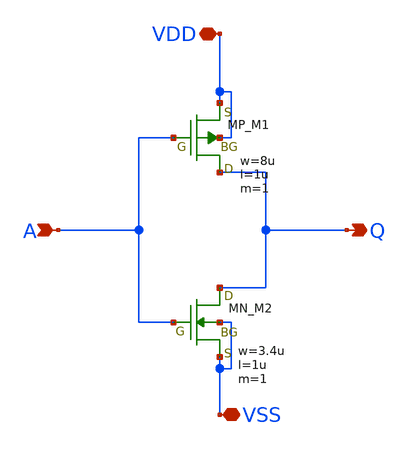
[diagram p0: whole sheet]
** sch_path: inverter_uneko_manu.sch
**.subckt inverter_uneko_manu A Q VDD VSS
*.ipin A
*.opin Q
*.iopin VDD
*.iopin VSS
XM1 Q A VDD VDD PMOS w=8u l=1u as=0 ad=0 ps=0 pd=0 nrd=0 nrs=0 m=1
XM2 Q A VSS VSS NMOS w=3.4u l=1u as=0 ad=0 ps=0 pd=0 nrd=0 nrs=0 m=1
**.ends
.end
